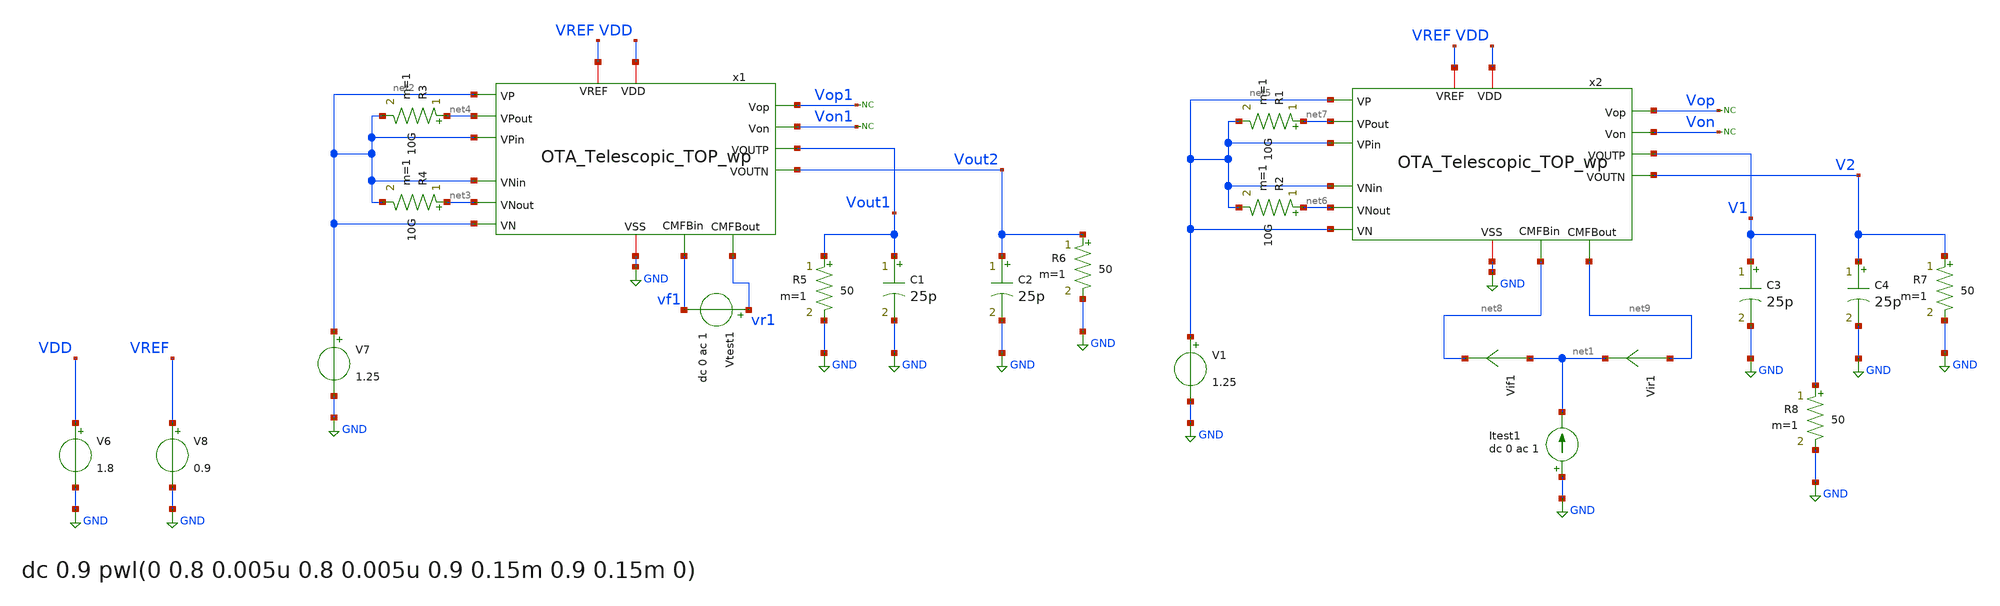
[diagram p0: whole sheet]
** sch_path: OTA_Telescopic_backup/OTA_Telescopic_NO_FLATTEN/Testbenchs/OTA_Telescopic_TOP_TB_CMFB.sch
**.subckt OTA_Telescopic_TOP_TB_CMFB
V7 net2 GND 1.25
C1 Vout1 GND 25p m=1
C2 Vout2 GND 25p m=1
V6 VDD GND 1.8
V8 VREF GND 0.9
Vtest1 vr1 vf1 dc 0 ac 1
Vif1 net1 net8 0
.save i(vif1)
Vir1 net9 net1 0
.save i(vir1)
Itest1 GND net1 dc 0 ac 1
R3 net4 net2 10G m=1
R4 net3 net2 10G m=1
V1 net5 GND 1.25
C3 V1 GND 25p m=1
C4 V2 GND 25p m=1
R1 net7 net5 10G m=1
R2 net6 net5 10G m=1
x1 VDD GND net4 net2 Vout1 net2 net2 Vout2 net2 net3 vf1 VREF vr1 Vop1 Von1 OTA_Telescopic_TOP_wp
x2 VDD GND net7 net5 V1 net5 net5 V2 net5 net6 net8 VREF net9 Vop Von OTA_Telescopic_TOP_wp
R5 Vout1 GND 50 m=1
R6 Vout2 GND 50 m=1
R7 V2 GND 50 m=1
R8 V1 GND 50 m=1
* noconn Vop1
* noconn Von1
* noconn Vop
* noconn Von
**** begin user architecture code

** opencircuitdesign pdks install
.lib cornerMOSlv.lib mos_tt
.lib cornerRES.lib res_typ
.lib cornerCAP.lib cap_typ
.temp 65




.options savecurrents reltol=1e-3 abstol=1e-12 gmin=1e-15
.control
save all
set color0 = white

* Operating Point Analysis
op
remzerovec
let cgg_M0 = @m.x1.xm0.msky130_fd_pr__nfet_01v8_lvt[cgg]
print cgg_M0
write OTA_Telescopic_TOP_TB_CMFB.raw
set appendwrite

* AC Analysis
ac dec 10 1 5G
remzerovec
write Middlebrook.raw
set appendwrite

* Middlebrook's Method
let tv=-v(vr1)/v(vf1)
let ti=-i(vir1)/i(vif1)
let tmb=(tv*ti - 1)/(tv + ti + 2)

let Av = db(tmb)
meas ac Ao MAX Av
let ABW = Ao-3
meas ac BW WHEN Av=ABW
meas ac UGBW WHEN Av=0

* Phase margin (PM)
let phase_vec= 180/pi*cph(tmb)
meas ac phase FIND phase_vec WHEN frequency=UGBW
let PM = phase+180
print PM

* Gain margin (GM)
meas ac freq180 FIND frequency WHEN phase_vec=-180
meas ac gain FIND Av WHEN frequency=freq180
let GM = 0-gain
print GM

plot Av ylabel 'Magnitude - Middlebrook'
plot phase_vec ylabel 'Phase - Middlebrook'

write Middlebrook_.raw

wrdata STB_Av_ Av
wrdata STB_ph_ phase_vec

*quit

.endc


**** end user architecture code
**.ends
.GLOBAL GND
.end
